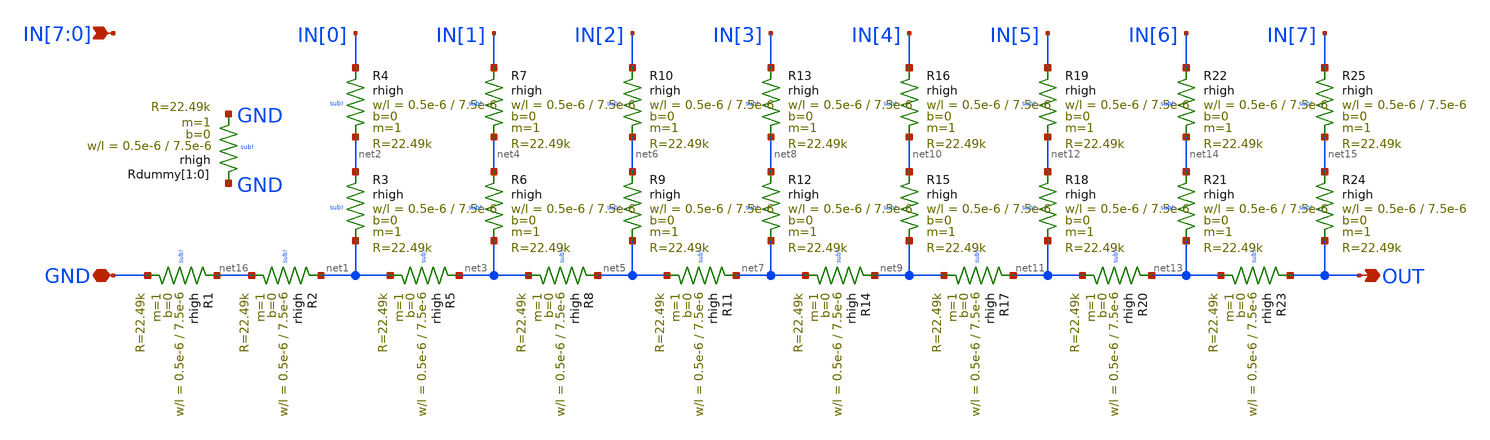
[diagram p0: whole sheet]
** sch_path: xschem/r2r_dac.sch
**.subckt r2r_dac GND IN[7],IN[6],IN[5],IN[4],IN[3],IN[2],IN[1],IN[0] OUT
*.iopin GND
*.ipin IN[7],IN[6],IN[5],IN[4],IN[3],IN[2],IN[1],IN[0]
*.opin OUT
XR1 net16 GND sub! rhigh w=0.5e-6 l=7.5e-6 m=1 b=0 mm_ok=1
XR3 net2 net1 sub! rhigh w=0.5e-6 l=7.5e-6 m=1 b=0 mm_ok=1
XR5 net3 net1 sub! rhigh w=0.5e-6 l=7.5e-6 m=1 b=0 mm_ok=1
XR6 net4 net3 sub! rhigh w=0.5e-6 l=7.5e-6 m=1 b=0 mm_ok=1
XR8 net5 net3 sub! rhigh w=0.5e-6 l=7.5e-6 m=1 b=0 mm_ok=1
XR9 net6 net5 sub! rhigh w=0.5e-6 l=7.5e-6 m=1 b=0 mm_ok=1
XR11 net7 net5 sub! rhigh w=0.5e-6 l=7.5e-6 m=1 b=0 mm_ok=1
XR12 net8 net7 sub! rhigh w=0.5e-6 l=7.5e-6 m=1 b=0 mm_ok=1
XR14 net9 net7 sub! rhigh w=0.5e-6 l=7.5e-6 m=1 b=0 mm_ok=1
XR15 net10 net9 sub! rhigh w=0.5e-6 l=7.5e-6 m=1 b=0 mm_ok=1
XR17 net11 net9 sub! rhigh w=0.5e-6 l=7.5e-6 m=1 b=0 mm_ok=1
XR18 net12 net11 sub! rhigh w=0.5e-6 l=7.5e-6 m=1 b=0 mm_ok=1
XR20 net13 net11 sub! rhigh w=0.5e-6 l=7.5e-6 m=1 b=0 mm_ok=1
XR21 net14 net13 sub! rhigh w=0.5e-6 l=7.5e-6 m=1 b=0 mm_ok=1
XR23 OUT net13 sub! rhigh w=0.5e-6 l=7.5e-6 m=1 b=0 mm_ok=1
XR24 net15 OUT sub! rhigh w=0.5e-6 l=7.5e-6 m=1 b=0 mm_ok=1
XR2 net1 net16 sub! rhigh w=0.5e-6 l=7.5e-6 m=1 b=0 mm_ok=1
XR4 IN[0] net2 sub! rhigh w=0.5e-6 l=7.5e-6 m=1 b=0 mm_ok=1
XR7 IN[1] net4 sub! rhigh w=0.5e-6 l=7.5e-6 m=1 b=0 mm_ok=1
XR10 IN[2] net6 sub! rhigh w=0.5e-6 l=7.5e-6 m=1 b=0 mm_ok=1
XR13 IN[3] net8 sub! rhigh w=0.5e-6 l=7.5e-6 m=1 b=0 mm_ok=1
XR16 IN[4] net10 sub! rhigh w=0.5e-6 l=7.5e-6 m=1 b=0 mm_ok=1
XR19 IN[5] net12 sub! rhigh w=0.5e-6 l=7.5e-6 m=1 b=0 mm_ok=1
XR22 IN[6] net14 sub! rhigh w=0.5e-6 l=7.5e-6 m=1 b=0 mm_ok=1
XR25 IN[7] net15 sub! rhigh w=0.5e-6 l=7.5e-6 m=1 b=0 mm_ok=1
XRdummy[1] GND GND sub! rhigh w=0.5e-6 l=7.5e-6 m=1 b=0 mm_ok=1
XRdummy[0] GND GND sub! rhigh w=0.5e-6 l=7.5e-6 m=1 b=0 mm_ok=1
**.ends
.end
